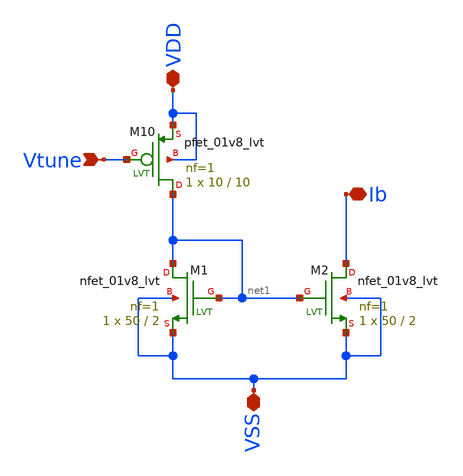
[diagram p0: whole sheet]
** sch_path: xschem/current_mirror/curr_mir.sch
**.subckt curr_mir VSS VDD Vtune Ib
*.iopin VSS
*.iopin VDD
*.ipin Vtune
*.iopin Ib
XM1 net1 net1 VSS VSS sky130_fd_pr__nfet_01v8_lvt L=2 W=50 nf=1 ad='int((1 + 1)/2) * 50 / 1 * 0.29' as='int((1 + 2)/2) * 50 / 1 * 0.29'
+ pd='2*int((1 + 1)/2) * (50 / 1 + 0.29)' ps='2*int((1 + 2)/2) * (50 / 1 + 0.29)' nrd='0.29 / 50 ' nrs='0.29 / 50 '
+ sa=0 sb=0 sd=0 mult=1 m=1
XM2 Ib net1 VSS VSS sky130_fd_pr__nfet_01v8_lvt L=2 W=50 nf=1 ad='int((1 + 1)/2) * 50 / 1 * 0.29' as='int((1 + 2)/2) * 50 / 1 * 0.29'
+ pd='2*int((1 + 1)/2) * (50 / 1 + 0.29)' ps='2*int((1 + 2)/2) * (50 / 1 + 0.29)' nrd='0.29 / 50 ' nrs='0.29 / 50 '
+ sa=0 sb=0 sd=0 mult=1 m=1
XM10 net1 Vtune VDD VDD sky130_fd_pr__pfet_01v8_lvt L=10 W=10 nf=1 ad='int((1 + 1)/2) * 10 / 1 * 0.29'
+ as='int((1 + 2)/2) * 10 / 1 * 0.29' pd='2*int((1 + 1)/2) * (10 / 1 + 0.29)' ps='2*int((1 + 2)/2) * (10 / 1 + 0.29)'
+ nrd='0.29 / 10 ' nrs='0.29 / 10 ' sa=0 sb=0 sd=0 mult=1 m=1
**.ends
.end
